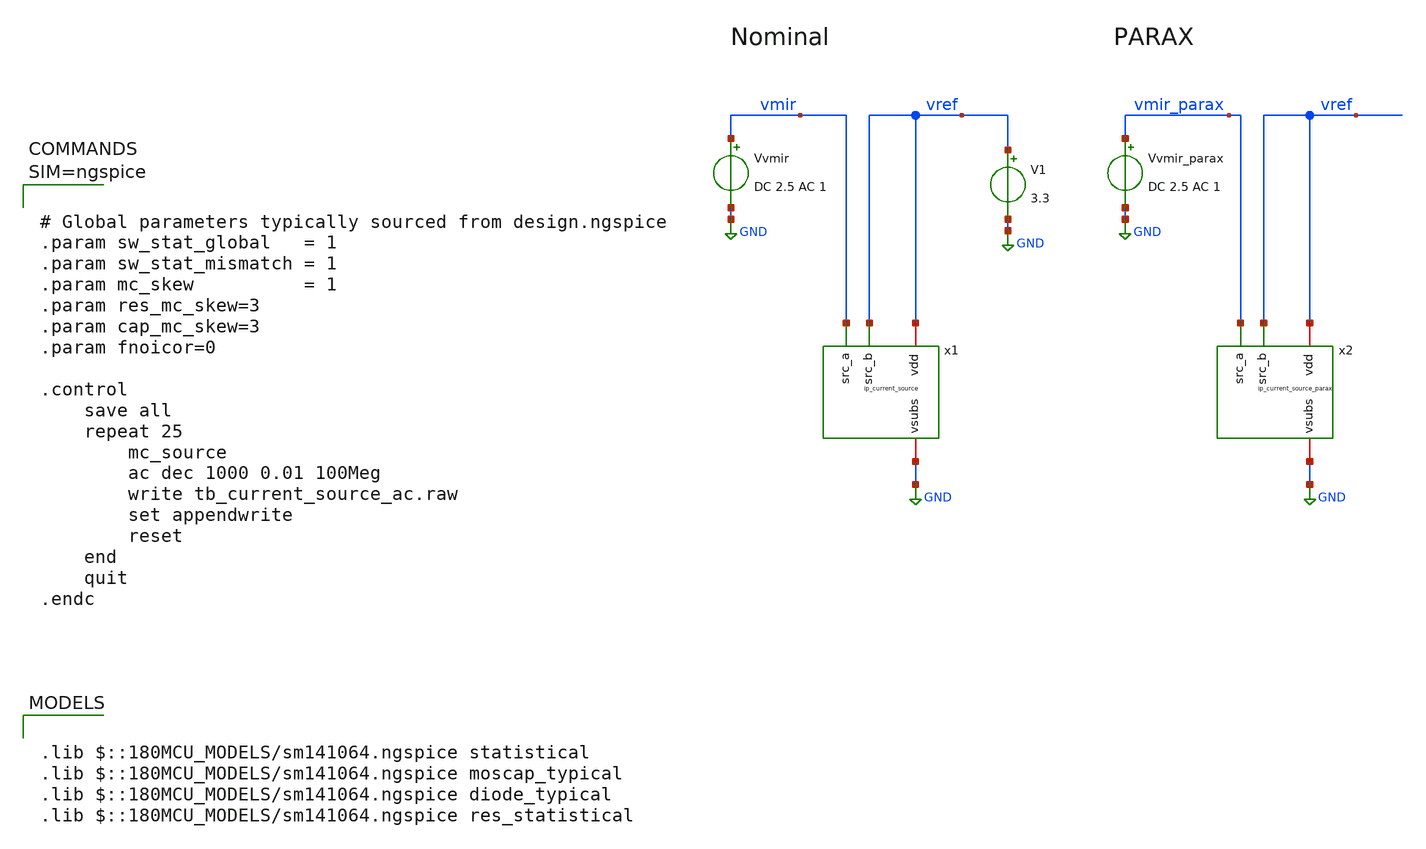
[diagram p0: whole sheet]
** sch_path: xschem/tb_current_source_ac.sch
**.subckt tb_current_source_ac
x1 vref vmir GND vref ip_current_source
V1 vref GND 3.3
Vvmir vmir GND DC 2.5 AC 1
x2 vref vmir_parax GND vref ip_current_source_parax
Vvmir_parax vmir_parax GND DC 2.5 AC 1
**** begin user architecture code

.lib $::180MCU_MODELS/sm141064.ngspice statistical
.lib $::180MCU_MODELS/sm141064.ngspice moscap_typical
.lib $::180MCU_MODELS/sm141064.ngspice diode_typical
.lib $::180MCU_MODELS/sm141064.ngspice res_statistical




# Global parameters typically sourced from design.ngspice
.param sw_stat_global   = 1
.param sw_stat_mismatch = 1
.param mc_skew          = 1
.param res_mc_skew=3
.param cap_mc_skew=3
.param fnoicor=0

.control
	save all
	repeat 25
		mc_source
		ac dec 1000 0.01 100Meg
		write tb_current_source_ac.raw
		set appendwrite
		reset
	end
	quit
.endc



**** end user architecture code
**.ends

* expanding   symbol:  ip_current_source.sym # of pins=4
** sym_path: xschem/ip_current_source.sym
** sch_path: xschem/ip_current_source.sch
.subckt ip_current_source vdd src_a vsubs src_b
*.iopin vdd
*.iopin vsubs
*.ipin src_a
*.ipin src_b
XM8 refin refin vsubs vsubs nfet_06v0 L=1u W=5u nf=1 ad='int((nf+1)/2) * W/nf * 0.18u' as='int((nf+2)/2) * W/nf * 0.18u'
+ pd='2*int((nf+1)/2) * (W/nf + 0.18u)' ps='2*int((nf+2)/2) * (W/nf + 0.18u)' nrd='0.18u / W' nrs='0.18u / W'
+ sa=0 sb=0 sd=0 m=1 par=1
XM5 src_a refin net1 vsubs nfet_06v0 L=0.7u W=5u nf=1 ad='int((nf+1)/2) * W/nf * 0.18u' as='int((nf+2)/2) * W/nf * 0.18u'
+ pd='2*int((nf+1)/2) * (W/nf + 0.18u)' ps='2*int((nf+2)/2) * (W/nf + 0.18u)' nrd='0.18u / W' nrs='0.18u / W'
+ sa=0 sb=0 sd=0 m=2 par=2
XM3 src_b refin net2 vsubs nfet_06v0 L=0.7u W=5u nf=1 ad='int((nf+1)/2) * W/nf * 0.18u' as='int((nf+2)/2) * W/nf * 0.18u'
+ pd='2*int((nf+1)/2) * (W/nf + 0.18u)' ps='2*int((nf+2)/2) * (W/nf + 0.18u)' nrd='0.18u / W' nrs='0.18u / W'
+ sa=0 sb=0 sd=0 m=2 par=2
XM4 net1 refin vsubs vsubs nfet_06v0 L=5u W=0.5u nf=1 ad='int((nf+1)/2) * W/nf * 0.18u' as='int((nf+2)/2) * W/nf * 0.18u'
+ pd='2*int((nf+1)/2) * (W/nf + 0.18u)' ps='2*int((nf+2)/2) * (W/nf + 0.18u)' nrd='0.18u / W' nrs='0.18u / W'
+ sa=0 sb=0 sd=0 m=1 par=1
XM7 net2 refin vsubs vsubs nfet_06v0 L=5u W=0.5u nf=1 ad='int((nf+1)/2) * W/nf * 0.18u' as='int((nf+2)/2) * W/nf * 0.18u'
+ pd='2*int((nf+1)/2) * (W/nf + 0.18u)' ps='2*int((nf+2)/2) * (W/nf + 0.18u)' nrd='0.18u / W' nrs='0.18u / W'
+ sa=0 sb=0 sd=0 m=1 par=1
XR5 refin vdd vsubs ppolyf_u_1k_6p0 r_width=1e-6 r_length=42e-6 m=1
.ends


* expanding   symbol:  ip_current_source_parax.sym # of pins=4
** sym_path: xschem/ip_current_source.sym
.include [file normalize ./parax/ip_current_source.sim.spice]
.GLOBAL GND
.end
